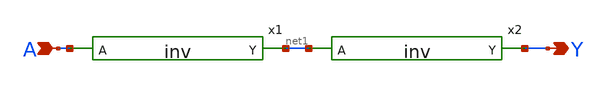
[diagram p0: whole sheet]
** sch_path: xschem/sim/buf.sch
**.subckt buf A Y
*.ipin A
*.opin Y
x1 A net1 inv
x2 net1 Y inv
**.ends

* expanding   symbol:  inv.sym # of pins=2
** sym_path: xschem/sim/inv.sym
** sch_path: xschem/sim/inv.sch
.subckt inv A Y
*.opin Y
*.ipin A
XM1 Y A VDD VDD sky130_fd_pr__pfet_01v8 L=0.15 W=1.26 nf=1 ad='int((nf+1)/2) * W/nf * 0.29' as='int((nf+2)/2) * W/nf * 0.29'
+ pd='2*int((nf+1)/2) * (W/nf + 0.29)' ps='2*int((nf+2)/2) * (W/nf + 0.29)' nrd='0.29 / W' nrs='0.29 / W'
+ sa=0 sb=0 sd=0 mult=1 m=1
XM2 Y A GND GND sky130_fd_pr__nfet_01v8 L=0.15 W=0.52 nf=1 ad='int((nf+1)/2) * W/nf * 0.29' as='int((nf+2)/2) * W/nf * 0.29'
+ pd='2*int((nf+1)/2) * (W/nf + 0.29)' ps='2*int((nf+2)/2) * (W/nf + 0.29)' nrd='0.29 / W' nrs='0.29 / W'
+ sa=0 sb=0 sd=0 mult=1 m=1
.ends

.GLOBAL VDD
.GLOBAL GND
.end
